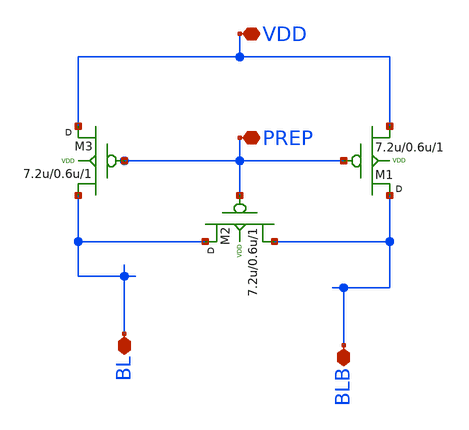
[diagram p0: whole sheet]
** sch_path: SRAM/precharge/schematic/precharge_schematic.sch
**.subckt precharge_schematic VDD BL BLB PREP
*.iopin VDD
*.iopin BL
*.iopin BLB
*.iopin PREP
M3 VDD PREP BL VDD pfet w=7.2u l=0.6u m=1
M1 BLB PREP VDD VDD pfet w=7.2u l=0.6u m=1
M2 BL PREP BLB VDD pfet w=7.2u l=0.6u m=1
**.ends
.end
